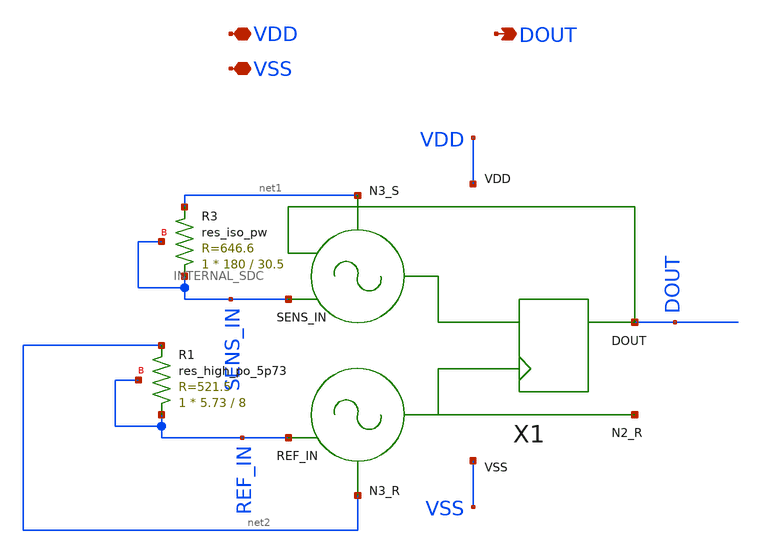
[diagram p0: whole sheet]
** sch_path: modules/SDC/symbol/SDC.sch
**.subckt SDC VDD VSS DOUT
*.iopin VDD
*.iopin VSS
*.opin DOUT
X1 SENS_IN REF_IN DOUT VDD VSS net1 net2 net3 INTERNAL_SDC
XR1 REF_IN net2 REF_IN sky130_fd_pr__res_high_po_5p73 L=8 mult=1 m=1
XR3 SENS_IN net1 SENS_IN sky130_fd_pr__res_iso_pw W=180 L=30.5 m=1
**.ends
.end
